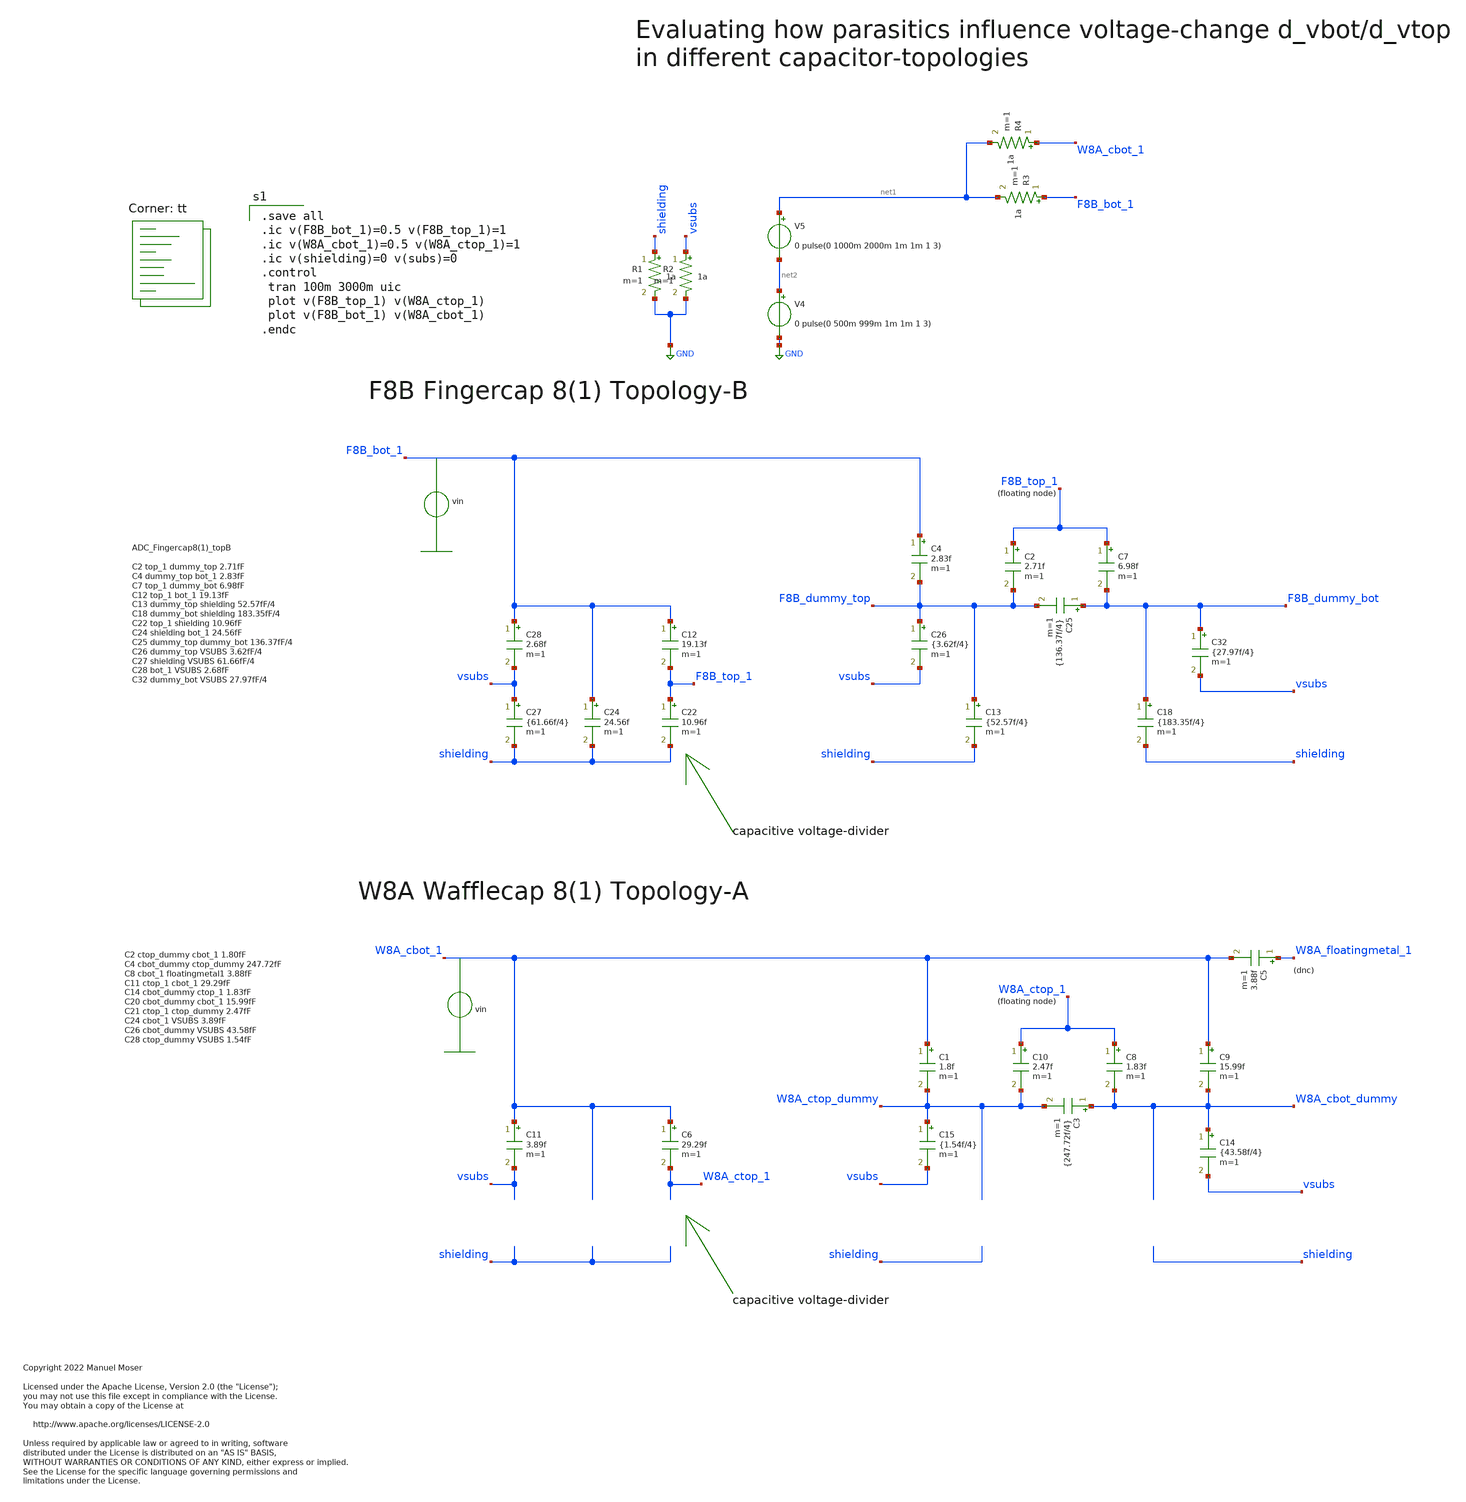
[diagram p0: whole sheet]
** sch_path: mag/adc_array_cap/parasitics.sch
* Copyright 2022 Manuel Moser
* Licensed under the Apache License, Version 2.0 (the "License");
**.subckt parasitics
C2 F8B_top_1 F8B_dummy_top 2.71f m=1
C4 F8B_bot_1 F8B_dummy_top 2.83f m=1
C7 F8B_top_1 F8B_dummy_bot 6.98f m=1
C12 F8B_bot_1 F8B_top_1 19.13f m=1
C13 F8B_dummy_top shielding {52.57f/4} m=1
C18 F8B_dummy_bot shielding {183.35f/4} m=1
C22 F8B_top_1 shielding 10.96f m=1
C24 F8B_bot_1 shielding 24.56f m=1
C25 F8B_dummy_bot F8B_dummy_top {136.37f/4} m=1
C26 F8B_dummy_top vsubs {3.62f/4} m=1
C27 vsubs shielding {61.66f/4} m=1
C28 F8B_bot_1 vsubs 2.68f m=1
C32 F8B_dummy_bot vsubs {27.97f/4} m=1
R1 shielding GND 1a m=1
R2 vsubs GND 1a m=1
V4 net2 GND 0 pulse(0 500m 999m 1m 1m 1 3)
C1 W8A_cbot_1 W8A_ctop_dummy 1.8f m=1
C3 W8A_cbot_dummy W8A_ctop_dummy {247.72f/4} m=1
C5 W8A_floatingmetal_1 W8A_cbot_1 3.88f m=1
C6 W8A_cbot_1 W8A_ctop_1 29.29f m=1
C8 W8A_ctop_1 W8A_cbot_dummy 1.83f m=1
C9 W8A_cbot_1 W8A_cbot_dummy 15.99f m=1
C10 W8A_ctop_1 W8A_ctop_dummy 2.47f m=1
C11 W8A_cbot_1 vsubs 3.89f m=1
C14 W8A_cbot_dummy vsubs {43.58f/4} m=1
C15 W8A_ctop_dummy vsubs {1.54f/4} m=1
R3 F8B_bot_1 net1 1a m=1
R4 W8A_cbot_1 net1 1a m=1
V5 net1 net2 0 pulse(0 1000m 2000m 1m 1m 1 3)
**** begin user architecture code

.save all
.ic v(F8B_bot_1)=0.5 v(F8B_top_1)=1
.ic v(W8A_cbot_1)=0.5 v(W8A_ctop_1)=1
.ic v(shielding)=0 v(subs)=0
.control
 tran 100m 3000m uic
 plot v(F8B_top_1) v(W8A_ctop_1)
 plot v(F8B_bot_1) v(W8A_cbot_1)
.endc

.lib $::SKYWATER_MODELS/sky130.lib.spice tt
**** end user architecture code
**.ends
.GLOBAL GND
.end
